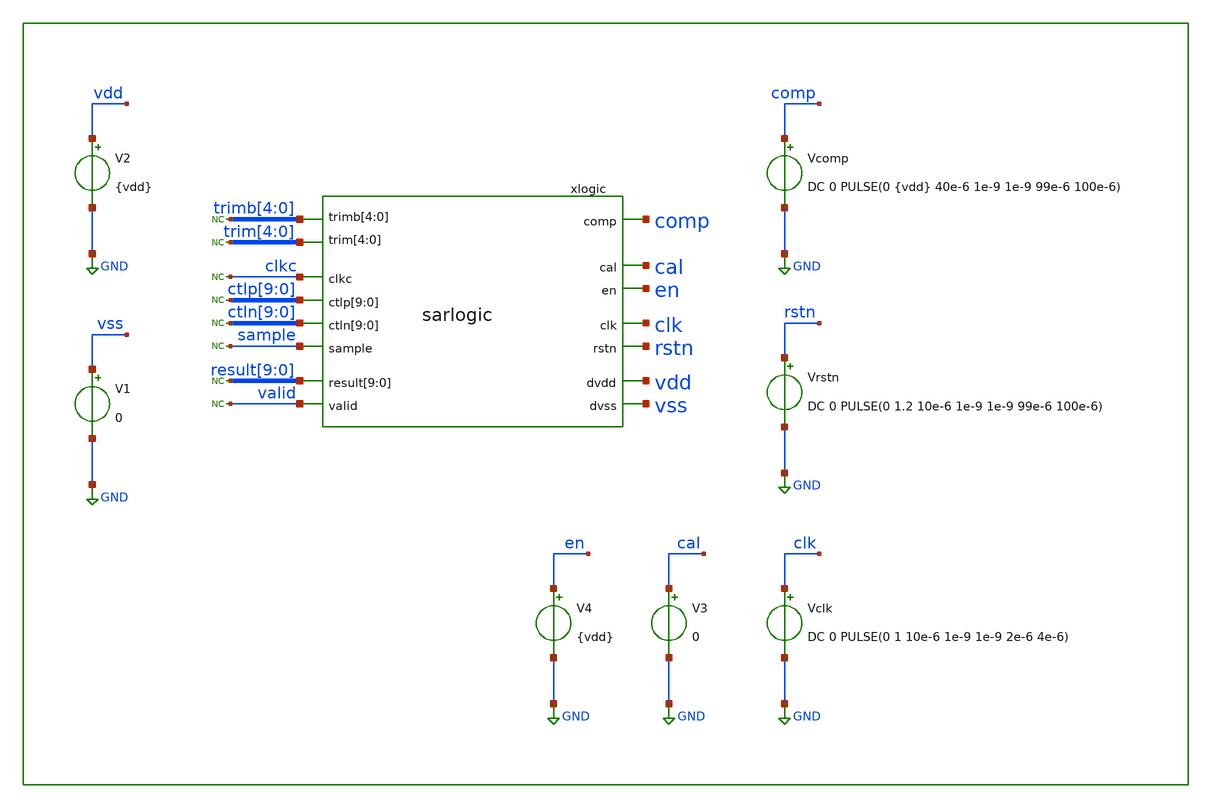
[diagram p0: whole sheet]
** sch_path: xschem/tb/sar_10b/tr_sarlogic.sch
**.subckt tr_sarlogic
V1 vss GND 0
V2 vdd GND {vdd}
Vclk clk GND DC 0 PULSE(0 1 10e-6 1e-9 1e-9 2e-6 4e-6)
V3 cal GND 0
Vrstn rstn GND DC 0 PULSE(0 1.2 10e-6 1e-9 1e-9 99e-6 100e-6)
xlogic trim[4] trim[3] trim[2] trim[1] trim[0] trimb[4] trimb[3] trimb[2] trimb[1] trimb[0] clkc
+ comp cal en ctlp[9] ctlp[8] ctlp[7] ctlp[6] ctlp[5] ctlp[4] ctlp[3] ctlp[2] ctlp[1] ctlp[0] clk
+ result[9] result[8] result[7] result[6] result[5] result[4] result[3] result[2] result[1] result[0] ctln[9]
+ ctln[8] ctln[7] ctln[6] ctln[5] ctln[4] ctln[3] ctln[2] ctln[1] ctln[0] valid rstn sample vdd vss sarlogic
* noconn trimb[4:0]
* noconn trim[4:0]
V4 en GND {vdd}
Vcomp comp GND DC 0 PULSE(0 {vdd} 40e-6 1e-9 1e-9 99e-6 100e-6)
* noconn clkc
* noconn ctlp[9:0]
* noconn ctln[9:0]
* noconn sample
* noconn result[9:0]
* noconn valid
**** begin user architecture code

.include $::SKYWATER_STDCELLS/cells/inv/sky130_fd_sc_hd__inv_4.spice
.include $::SKYWATER_STDCELLS/cells/decap/sky130_fd_sc_hd__decap_8.spice
.include $::SKYWATER_STDCELLS/cells/decap/sky130_fd_sc_hd__decap_3.spice
.include $::SKYWATER_STDCELLS/cells/buf/sky130_fd_sc_hd__buf_1.spice
.include $::SKYWATER_STDCELLS/cells/inv/sky130_fd_sc_hd__inv_1.spice
.include $::SKYWATER_STDCELLS/cells/inv/sky130_fd_sc_hd__inv_2.spice
.include $::SKYWATER_STDCELLS/cells/tap/sky130_fd_sc_hd__tap_2.spice
 *.options method = trap
*.options gmin   = 1e-12
*.options abstol = 1e-8
*.options chtol  = 1e-18
*.options reltol = 0.01
*.options vntol  = 0.1e-6

*.options rshunt = 10e-12

.param MC_SWITCH=0

.ic v(valid)=0
.ic v(sample)=0
.ic v(clkc)=0

.ic v(trim_0_)=0
.ic v(trim_1_)=0
.ic v(trim_2_)=0
.ic v(trim_3_)=0
.ic v(trim_4_)=0
.ic v(trimb_0_)=0
.ic v(trimb_1_)=0
.ic v(trimb_2_)=0
.ic v(trimb_3_)=0
.ic v(trimb_4_)=0


.ic v(result_0_)=0
.ic v(result_1_)=0
.ic v(result_2_)=0
.ic v(result_3_)=0
.ic v(result_4_)=0
.ic v(result_5_)=0
.ic v(result_6_)=0
.ic v(result_7_)=0
.ic v(result_8_)=0
.ic v(result_9_)=0

.ic v(ctlp_0_)=0
.ic v(ctlp_1_)=0
.ic v(ctlp_2_)=0
.ic v(ctlp_3_)=0
.ic v(ctlp_4_)=0
.ic v(ctlp_5_)=0
.ic v(ctlp_6_)=0
.ic v(ctlp_7_)=0
.ic v(ctlp_8_)=0
.ic v(ctlp_9_)=0

.ic v(ctln_0_)=0
.ic v(ctln_1_)=0
.ic v(ctln_2_)=0
.ic v(ctln_3_)=0
.ic v(ctln_4_)=0
.ic v(ctln_5_)=0
.ic v(ctln_6_)=0
.ic v(ctln_7_)=0
.ic v(ctln_8_)=0
.ic v(ctln_9_)=0

.include $::DESIGN_PATH/sar_10b/control/sarlogic.ext.spice

.param vdd=1.2

*.tran 100e-9 68e-6
.tran 100e-9 68e-6 uic

save clkc

.control
run

echo Simulation Finished
echo -------------------
shell date
echo -------------------

.endc

 * FET CORNERS
.include $::SKYWATER_MODELS/models/corners/tt.spice
*.include $::SKYWATER_MODELS/corners/ff.spice
*.include $::SKYWATER_MODELS/corners/ss.spice
*.include $::SKYWATER_MODELS/corners/sf.spice
*.include $::SKYWATER_MODELS/corners/fs.spice

* TT + R + C
*.include $::SKYWATER_MODELS/corners/tt_rmax_cmax.spice
*.include $::SKYWATER_MODELS/corners/tt_rmin_cmin.spice
*.include $::SKYWATER_MODELS/corners/tt_rmax_cmin.spice
*.include $::SKYWATER_MODELS/corners/tt_rmin_cmax.spice

* FF + R + C
*.include $::SKYWATER_MODELS/corners/ff_rmax_cmax.spice
*.include $::SKYWATER_MODELS/corners/ff_rmin_cmin.spice
*.include $::SKYWATER_MODELS/corners/ff_rmax_cmin.spice
*.include $::SKYWATER_MODELS/corners/ff_rmin_cmax.spice


* SS + R + C
*.include $::SKYWATER_MODELS/corners/ss_rmax_cmax.spice
*.include $::SKYWATER_MODELS/corners/ss_rmin_cmin.spice
*.include $::SKYWATER_MODELS/corners/ss_rmax_cmin.spice
*.include $::SKYWATER_MODELS/corners/ss_rmin_cmax.spice

* SF + R + C
*.include $::SKYWATER_MODELS/corners/sf_rmax_cmax.spice
*.include $::SKYWATER_MODELS/corners/sf_rmin_cmin.spice
*.include $::SKYWATER_MODELS/corners/sf_rmax_cmin.spice
*.include $::SKYWATER_MODELS/corners/sf_rmin_cmax.spice

* FS + R + C
*.include $::SKYWATER_MODELS/corners/fs_rmax_cmax.spice
*.include $::SKYWATER_MODELS/corners/fs_rmin_cmin.spice
*.include $::SKYWATER_MODELS/corners/fs_rmax_cmin.spice
*.include $::SKYWATER_MODELS/corners/fs_rmin_cmax.spice
**** end user architecture code
**.ends

* expanding   symbol:  sar_10b/control/sarlogic.sym # of pins=15
** sym_path: sar_10b/control/sarlogic.sym
** sch_path: sar_10b/control/sarlogic.sch
.subckt sarlogic trim[4] trim[3] trim[2] trim[1] trim[0] trimb[4] trimb[3] trimb[2] trimb[1]
+ trimb[0] clkc comp cal en ctlp[9] ctlp[8] ctlp[7] ctlp[6] ctlp[5] ctlp[4] ctlp[3] ctlp[2] ctlp[1] ctlp[0]
+ clk result[9] result[8] result[7] result[6] result[5] result[4] result[3] result[2] result[1] result[0]
+ ctln[9] ctln[8] ctln[7] ctln[6] ctln[5] ctln[4] ctln[3] ctln[2] ctln[1] ctln[0] valid rstn sample dvdd dvss
*.opin clkc
*.opin ctlp[9],ctlp[8],ctlp[7],ctlp[6],ctlp[5],ctlp[4],ctlp[3],ctlp[2],ctlp[1],ctlp[0]
*.opin ctln[9],ctln[8],ctln[7],ctln[6],ctln[5],ctln[4],ctln[3],ctln[2],ctln[1],ctln[0]
*.opin sample
*.opin trim[4],trim[3],trim[2],trim[1],trim[0]
*.opin trimb[4],trimb[3],trimb[2],trimb[1],trimb[0]
*.ipin comp
*.ipin cal
*.ipin en
*.ipin clk
*.ipin
*+ result[9],result[8],result[7],result[6],result[5],result[4],result[3],result[2],result[1],result[0]
*.ipin valid
*.ipin rstn
*.iopin dvdd
*.iopin dvss
* noconn comp
* noconn ctlp[9:0]
* noconn ctln[9:0]
* noconn sample
* noconn trimb[4:0]
* noconn trim[4:0]
* noconn result[9:0]
* noconn valid
* noconn clkc
* noconn clk
* noconn en
* noconn cal
* noconn rstn
**** begin user architecture code
.include $::DESIGN_PATH/sar_10b/control/cmos_cells_digital.sp
.include $::DESIGN_PATH/sar_10b/control/sarlogic.sp

**** end user architecture code
* noconn dvdd
* noconn dvss
**** begin user architecture code
* Keep the sar_logic underscore name. Otherwise xschem gets confused.
Xuut dclk drstn den dcomp dcal dvalid dres0 dres1 dres2 dres3 dres4 dres5 dres6 dres7 dres8 dres9
+ dsamp dctlp0 dctlp1 dctlp2 dctlp3 dctlp4 dctlp5 dctlp6 dctlp7 dctlp8 dctlp9 dctln0 dctln1 dctln2 dctln3
+ dctln4 dctln5 dctln6 dctln7 dctln8 dctln9 dtrim0 dtrim1 dtrim2 dtrim3 dtrim4 dtrimb0 dtrimb1 dtrimb2
+ dtrimb3 dtrimb4 dclkc sar_logic

.model adc_buff adc_bridge(in_low = 0.2 in_high=0.8)
.model dac_buff dac_bridge(out_high = 1.2)

Aad [clk rstn en comp cal] [dclk drstn den dcomp dcal] adc_buff
Ada1 [dctlp0 dctlp1 dctlp2 dctlp3 dctlp4 dctlp5 dctlp6 dctlp7 dctlp8 dctlp9] [ctlp_0_ ctlp_1_
+ ctlp_2_ ctlp_3_ ctlp_4_ ctlp_5_ ctlp_6_ ctlp_7_ ctlp_8_ ctlp_9_] dac_buff
Ada2 [dctln0 dctln1 dctln2 dctln3 dctln4 dctln5 dctln6 dctln7 dctln8 dctln9] [ctln_0_ ctln_1_
+ ctln_2_ ctln_3_ ctln_4_ ctln_5_ ctln_6_ ctln_7_ ctln_8_ ctln_9_] dac_buff
Ada3 [dres0 dres1 dres2 dres3 dres4 dres5 dres6 dres7 dres8 dres9 dsamp dclkc] [res0 res1 res2 res3
+ res4 res5 res6 res7 res8 res9 sample clkc] dac_buff
Ada4 [dtrim4 dtrim3 dtrim2 dtrim1 dtrim0 dtrimb4 dtrimb3 dtrimb2 dtrimb1 dtrimb0] [trim_4_ trim_3_
+ trim_2_ trim_1_ trim_0_ trimb_4_ trimb_3_ trimb_2_ trimb_1_ trimb_0_ ] dac_buff

**** end user architecture code
.ends

.GLOBAL GND
.end
